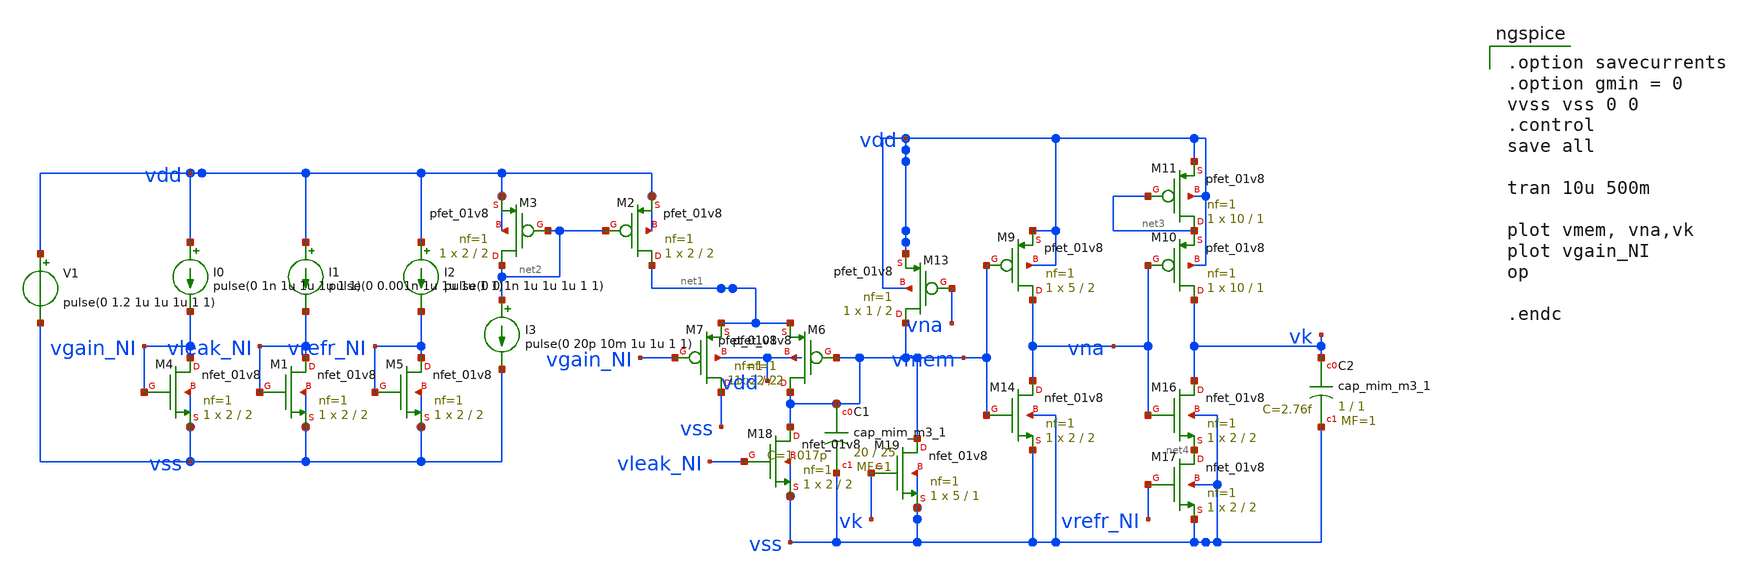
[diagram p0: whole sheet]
** sch_path: circuits/DPI_tb.sch
* Copyright 2020 Stefan Frederik Schippers
* Licensed under the Apache License, Version 2.0 (the "License");
* you may not use this file except in compliance with the License.
* You may obtain a copy of the License at
* https://www.apache.org/licenses/LICENSE-2.0
* Unless required by applicable law or agreed to in writing, software
* distributed under the License is distributed on an "AS IS" BASIS,
* WITHOUT WARRANTIES OR CONDITIONS OF ANY KIND, either express or implied.
* See the License for the specific language governing permissions and
* limitations under the License.
**.subckt DPI_tb
XM2 net1 net2 vdd vdd sky130_fd_pr__pfet_01v8 L=2 W=2 nf=1 ad='int((nf+1)/2) * W/nf * 0.29' as='int((nf+2)/2) * W/nf * 0.29'
+ pd='2*int((nf+1)/2) * (W/nf + 0.29)' ps='2*int((nf+2)/2) * (W/nf + 0.29)' nrd='0.29 / W' nrs='0.29 / W'
+ sa=0 sb=0 sd=0 mult=1 m=1
XM3 net2 net2 vdd vdd sky130_fd_pr__pfet_01v8 L=2 W=2 nf=1 ad='int((nf+1)/2) * W/nf * 0.29' as='int((nf+2)/2) * W/nf * 0.29'
+ pd='2*int((nf+1)/2) * (W/nf + 0.29)' ps='2*int((nf+2)/2) * (W/nf + 0.29)' nrd='0.29 / W' nrs='0.29 / W'
+ sa=0 sb=0 sd=0 mult=1 m=1
XM5 vrefr_NI vrefr_NI vss vss sky130_fd_pr__nfet_01v8 L=2 W=2 nf=1 ad='int((nf+1)/2) * W/nf * 0.29' as='int((nf+2)/2) * W/nf * 0.29'
+ pd='2*int((nf+1)/2) * (W/nf + 0.29)' ps='2*int((nf+2)/2) * (W/nf + 0.29)' nrd='0.29 / W' nrs='0.29 / W'
+ sa=0 sb=0 sd=0 mult=1 m=1
XM1 vleak_NI vleak_NI vss vss sky130_fd_pr__nfet_01v8 L=2 W=2 nf=1 ad='int((nf+1)/2) * W/nf * 0.29' as='int((nf+2)/2) * W/nf * 0.29'
+ pd='2*int((nf+1)/2) * (W/nf + 0.29)' ps='2*int((nf+2)/2) * (W/nf + 0.29)' nrd='0.29 / W' nrs='0.29 / W'
+ sa=0 sb=0 sd=0 mult=1 m=1
XM4 vgain_NI vgain_NI vss vss sky130_fd_pr__nfet_01v8 L=2 W=2 nf=1 ad='int((nf+1)/2) * W/nf * 0.29' as='int((nf+2)/2) * W/nf * 0.29'
+ pd='2*int((nf+1)/2) * (W/nf + 0.29)' ps='2*int((nf+2)/2) * (W/nf + 0.29)' nrd='0.29 / W' nrs='0.29 / W'
+ sa=0 sb=0 sd=0 mult=1 m=1
I0 vdd vgain_NI pulse(0 1n 1u 1u 1u 1 1)
I1 vdd vleak_NI pulse(0 0.001n 1u 1u 1u 1 1)
I2 vdd vrefr_NI pulse(0 0.1n 1u 1u 1u 1 1)
I3 net2 vss pulse(0 20p 10m 1u 1u 1 1)
V1 vdd vss pulse(0 1.2 1u 1u 1u 1 1)
XM6 vmem vmem net1 vdd sky130_fd_pr__pfet_01v8 L=2 W=2 nf=1 ad='int((nf+1)/2) * W/nf * 0.29' as='int((nf+2)/2) * W/nf * 0.29'
+ pd='2*int((nf+1)/2) * (W/nf + 0.29)' ps='2*int((nf+2)/2) * (W/nf + 0.29)' nrd='0.29 / W' nrs='0.29 / W'
+ sa=0 sb=0 sd=0 mult=1 m=1
XM7 vss vgain_NI net1 vdd sky130_fd_pr__pfet_01v8 L=2 W=2 nf=1 ad='int((nf+1)/2) * W/nf * 0.29' as='int((nf+2)/2) * W/nf * 0.29'
+ pd='2*int((nf+1)/2) * (W/nf + 0.29)' ps='2*int((nf+2)/2) * (W/nf + 0.29)' nrd='0.29 / W' nrs='0.29 / W'
+ sa=0 sb=0 sd=0 mult=1 m=1
XM9 vna vmem vdd vdd sky130_fd_pr__pfet_01v8 L=2 W=5 nf=1 ad='int((nf+1)/2) * W/nf * 0.29' as='int((nf+2)/2) * W/nf * 0.29'
+ pd='2*int((nf+1)/2) * (W/nf + 0.29)' ps='2*int((nf+2)/2) * (W/nf + 0.29)' nrd='0.29 / W' nrs='0.29 / W'
+ sa=0 sb=0 sd=0 mult=1 m=1
XM10 vk vna net3 vdd sky130_fd_pr__pfet_01v8 L=1 W=10 nf=1 ad='int((nf+1)/2) * W/nf * 0.29' as='int((nf+2)/2) * W/nf * 0.29'
+ pd='2*int((nf+1)/2) * (W/nf + 0.29)' ps='2*int((nf+2)/2) * (W/nf + 0.29)' nrd='0.29 / W' nrs='0.29 / W'
+ sa=0 sb=0 sd=0 mult=1 m=1
XM11 net3 net3 vdd vdd sky130_fd_pr__pfet_01v8 L=1 W=10 nf=1 ad='int((nf+1)/2) * W/nf * 0.29' as='int((nf+2)/2) * W/nf * 0.29'
+ pd='2*int((nf+1)/2) * (W/nf + 0.29)' ps='2*int((nf+2)/2) * (W/nf + 0.29)' nrd='0.29 / W' nrs='0.29 / W'
+ sa=0 sb=0 sd=0 mult=1 m=1
XM13 vmem vna vdd vdd sky130_fd_pr__pfet_01v8 L=2 W=1 nf=1 ad='int((nf+1)/2) * W/nf * 0.29' as='int((nf+2)/2) * W/nf * 0.29'
+ pd='2*int((nf+1)/2) * (W/nf + 0.29)' ps='2*int((nf+2)/2) * (W/nf + 0.29)' nrd='0.29 / W' nrs='0.29 / W'
+ sa=0 sb=0 sd=0 mult=1 m=1
XM14 vna vmem vss vss sky130_fd_pr__nfet_01v8 L=2 W=2 nf=1 ad='int((nf+1)/2) * W/nf * 0.29' as='int((nf+2)/2) * W/nf * 0.29'
+ pd='2*int((nf+1)/2) * (W/nf + 0.29)' ps='2*int((nf+2)/2) * (W/nf + 0.29)' nrd='0.29 / W' nrs='0.29 / W'
+ sa=0 sb=0 sd=0 mult=1 m=1
XM16 vk vna net4 vss sky130_fd_pr__nfet_01v8 L=2 W=2 nf=1 ad='int((nf+1)/2) * W/nf * 0.29' as='int((nf+2)/2) * W/nf * 0.29'
+ pd='2*int((nf+1)/2) * (W/nf + 0.29)' ps='2*int((nf+2)/2) * (W/nf + 0.29)' nrd='0.29 / W' nrs='0.29 / W'
+ sa=0 sb=0 sd=0 mult=1 m=1
XM17 net4 vrefr_NI vss vss sky130_fd_pr__nfet_01v8 L=2 W=2 nf=1 ad='int((nf+1)/2) * W/nf * 0.29' as='int((nf+2)/2) * W/nf * 0.29'
+ pd='2*int((nf+1)/2) * (W/nf + 0.29)' ps='2*int((nf+2)/2) * (W/nf + 0.29)' nrd='0.29 / W' nrs='0.29 / W'
+ sa=0 sb=0 sd=0 mult=1 m=1
XM18 vmem vleak_NI vss vss sky130_fd_pr__nfet_01v8 L=2 W=2 nf=1 ad='int((nf+1)/2) * W/nf * 0.29' as='int((nf+2)/2) * W/nf * 0.29'
+ pd='2*int((nf+1)/2) * (W/nf + 0.29)' ps='2*int((nf+2)/2) * (W/nf + 0.29)' nrd='0.29 / W' nrs='0.29 / W'
+ sa=0 sb=0 sd=0 mult=1 m=1
XM19 vmem vk vss vss sky130_fd_pr__nfet_01v8 L=1 W=5 nf=1 ad='int((nf+1)/2) * W/nf * 0.29' as='int((nf+2)/2) * W/nf * 0.29'
+ pd='2*int((nf+1)/2) * (W/nf + 0.29)' ps='2*int((nf+2)/2) * (W/nf + 0.29)' nrd='0.29 / W' nrs='0.29 / W'
+ sa=0 sb=0 sd=0 mult=1 m=1
XC1 vmem vss sky130_fd_pr__cap_mim_m3_1 W=20 L=25 MF=1 m=1
XC2 vk vss sky130_fd_pr__cap_mim_m3_1 W=1 L=1 MF=1 m=1
**** begin user architecture code
 .lib $::SKYWATER_MODELS/models/sky130.lib.spice tt

.param mc_mm_switch=0
.param mc_pr_switch=1



.option savecurrents
.option gmin = 0
vvss vss 0 0
.control
save all

tran 10u 500m

plot vmem, vna,vk
plot vgain_NI
op

.endc


**** end user architecture code
**.ends
.end
